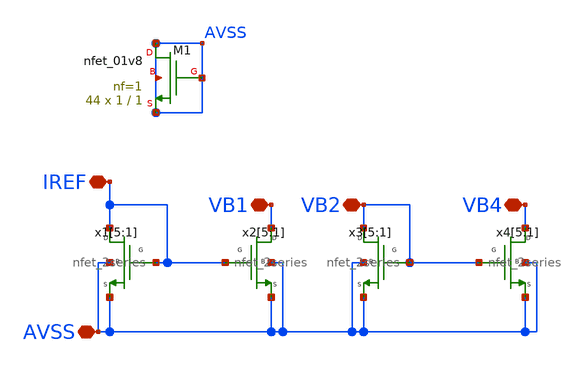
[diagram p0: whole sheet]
** sch_path: INA_layout_v2/bias/nbias_vb124.sch
**.subckt nbias_vb124 IREF VB1 VB2 VB4 AVSS
*.iopin IREF
*.iopin VB1
*.iopin VB2
*.iopin VB4
*.iopin AVSS
x1[5] AVSS AVSS IREF IREF nfet_2series
x1[4] AVSS AVSS IREF IREF nfet_2series
x1[3] AVSS AVSS IREF IREF nfet_2series
x1[2] AVSS AVSS IREF IREF nfet_2series
x1[1] AVSS AVSS IREF IREF nfet_2series
x2[5] AVSS AVSS IREF VB1 nfet_2series
x2[4] AVSS AVSS IREF VB1 nfet_2series
x2[3] AVSS AVSS IREF VB1 nfet_2series
x2[2] AVSS AVSS IREF VB1 nfet_2series
x2[1] AVSS AVSS IREF VB1 nfet_2series
x3[5] AVSS AVSS VB2 VB2 nfet_2series
x3[4] AVSS AVSS VB2 VB2 nfet_2series
x3[3] AVSS AVSS VB2 VB2 nfet_2series
x3[2] AVSS AVSS VB2 VB2 nfet_2series
x3[1] AVSS AVSS VB2 VB2 nfet_2series
x4[5] AVSS AVSS VB2 VB4 nfet_2series
x4[4] AVSS AVSS VB2 VB4 nfet_2series
x4[3] AVSS AVSS VB2 VB4 nfet_2series
x4[2] AVSS AVSS VB2 VB4 nfet_2series
x4[1] AVSS AVSS VB2 VB4 nfet_2series
XM1 AVSS AVSS AVSS AVSS sky130_fd_pr__nfet_01v8 L=1 W=1 nf=1 ad='int((nf+1)/2) * W/nf * 0.29' as='int((nf+2)/2) * W/nf * 0.29'
+ pd='2*int((nf+1)/2) * (W/nf + 0.29)' ps='2*int((nf+2)/2) * (W/nf + 0.29)' nrd='0.29 / W' nrs='0.29 / W'
+ sa=0 sb=0 sd=0 mult=44 m=44
**.ends

* expanding   symbol:  INA_layout_v2/bias/nfet_2series.sym # of pins=4
** sym_path: INA_layout_v2/bias/nfet_2series.sym
** sch_path: INA_layout_v2/bias/nfet_2series.sch
.subckt nfet_2series S B G D
*.iopin S
*.iopin B
*.iopin G
*.iopin D
XM1 D G net1 B sky130_fd_pr__nfet_01v8 L=1 W=1 nf=1 ad='int((nf+1)/2) * W/nf * 0.29' as='int((nf+2)/2) * W/nf * 0.29'
+ pd='2*int((nf+1)/2) * (W/nf + 0.29)' ps='2*int((nf+2)/2) * (W/nf + 0.29)' nrd='0.29 / W' nrs='0.29 / W'
+ sa=0 sb=0 sd=0 mult=1 m=1
XM2 net1 G S B sky130_fd_pr__nfet_01v8 L=1 W=1 nf=1 ad='int((nf+1)/2) * W/nf * 0.29' as='int((nf+2)/2) * W/nf * 0.29'
+ pd='2*int((nf+1)/2) * (W/nf + 0.29)' ps='2*int((nf+2)/2) * (W/nf + 0.29)' nrd='0.29 / W' nrs='0.29 / W'
+ sa=0 sb=0 sd=0 mult=1 m=1
.ends

.end
